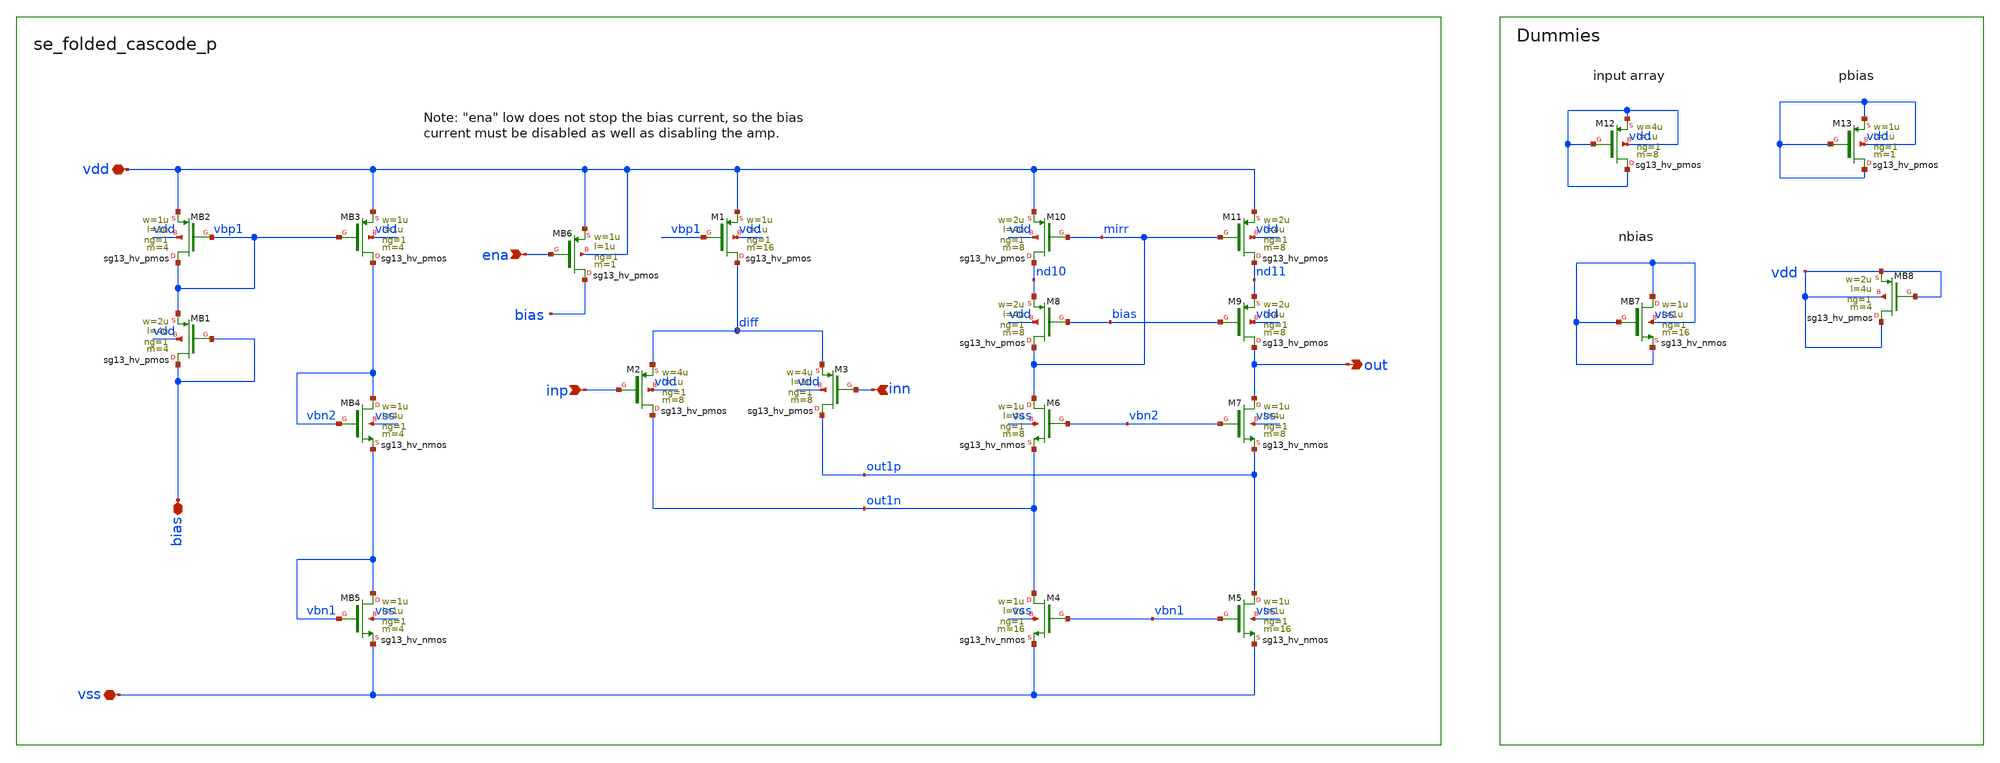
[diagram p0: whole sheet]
** sch_path: xschem/se_folded_cascode_p.sch
**.subckt se_folded_cascode_p inn inp out bias vdd vss ena
*.ipin inn
*.ipin inp
*.opin out
*.iopin bias
*.iopin vdd
*.iopin vss
*.ipin ena
XM3 out1p inn diff vdd sg13_hv_pmos w=4u l=1u ng=1 m=8 mm_ok=1
XM2 out1n inp diff vdd sg13_hv_pmos w=4u l=1u ng=1 m=8 mm_ok=1
XM1 diff vbp1 vdd vdd sg13_hv_pmos w=1u l=1u ng=1 m=16 mm_ok=1
XM4 out1n vbn1 vss vss sg13_hv_nmos w=1u l=1u ng=1 m=16 mm_ok=1
XM5 out1p vbn1 vss vss sg13_hv_nmos w=1u l=1u ng=1 m=16 mm_ok=1
XM6 mirr vbn2 out1n vss sg13_hv_nmos w=1u l=4u ng=1 m=8 mm_ok=1
XM7 out vbn2 out1p vss sg13_hv_nmos w=1u l=4u ng=1 m=8 mm_ok=1
XM8 mirr bias nd10 vdd sg13_hv_pmos w=2u l=4u ng=1 m=8 mm_ok=1
XM9 out bias nd11 vdd sg13_hv_pmos w=2u l=4u ng=1 m=8 mm_ok=1
XM10 nd10 mirr vdd vdd sg13_hv_pmos w=2u l=4u ng=1 m=8 mm_ok=1
XM11 nd11 mirr vdd vdd sg13_hv_pmos w=2u l=4u ng=1 m=8 mm_ok=1
XMB1 bias bias vbp1 vdd sg13_hv_pmos w=2u l=4u ng=1 m=4 mm_ok=1
XMB2 vbp1 vbp1 vdd vdd sg13_hv_pmos w=1u l=1u ng=1 m=4 mm_ok=1
XMB3 vbn2 vbp1 vdd vdd sg13_hv_pmos w=1u l=1u ng=1 m=4 mm_ok=1
XMB4 vbn2 vbn2 vbn1 vss sg13_hv_nmos w=1u l=4u ng=1 m=4 mm_ok=1
XMB5 vbn1 vbn1 vss vss sg13_hv_nmos w=1u l=1u ng=1 m=4 mm_ok=1
XMB6 bias ena vdd vdd sg13_hv_pmos w=1u l=1u ng=1 m=1 mm_ok=1
XM12 vdd vdd vdd vdd sg13_hv_pmos w=4u l=1u ng=1 m=8 mm_ok=1
XM13 vdd vdd vdd vdd sg13_hv_pmos w=1u l=1u ng=1 m=1 mm_ok=1
XMB7 vss vss vss vss sg13_hv_nmos w=1u l=1u ng=1 m=16 mm_ok=1
XMB8 vdd vdd vdd vdd sg13_hv_pmos w=2u l=4u ng=1 m=4 mm_ok=1
**.ends
.end
